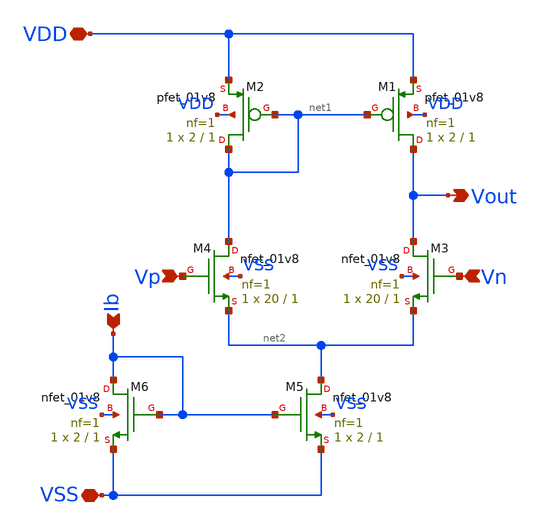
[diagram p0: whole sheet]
** sch_path: xschem/ota-5t.sch
**.subckt ota-5t Vp Vn Vout VDD VSS Ib
*.ipin Vp
*.ipin Vn
*.opin Vout
*.iopin VDD
*.iopin VSS
*.ipin Ib
XM4 net1 Vp net2 VSS sky130_fd_pr__nfet_01v8 L=1 W=20 nf=1 ad='int((1 + 1)/2) * 20 / 1 * 0.29' as='int((1 + 2)/2) * 20 / 1 * 0.29'
+ pd='2*int((1 + 1)/2) * (20 / 1 + 0.29)' ps='2*int((1 + 2)/2) * (20 / 1 + 0.29)' nrd='0.29 / 20 ' nrs='0.29 / 20 '
+ sa=0 sb=0 sd=0 mult=1 m=1
XM1 Vout net1 VDD VDD sky130_fd_pr__pfet_01v8 L=1 W=2 nf=1 ad='int((nf+1)/2) * W/nf * 0.29' as='int((nf+2)/2) * W/nf * 0.29'
+ pd='2*int((nf+1)/2) * (W/nf + 0.29)' ps='2*int((nf+2)/2) * (W/nf + 0.29)' nrd='0.29 / W' nrs='0.29 / W'
+ sa=0 sb=0 sd=0 mult=1 m=1
XM2 net1 net1 VDD VDD sky130_fd_pr__pfet_01v8 L=1 W=2 nf=1 ad='int((nf+1)/2) * W/nf * 0.29' as='int((nf+2)/2) * W/nf * 0.29'
+ pd='2*int((nf+1)/2) * (W/nf + 0.29)' ps='2*int((nf+2)/2) * (W/nf + 0.29)' nrd='0.29 / W' nrs='0.29 / W'
+ sa=0 sb=0 sd=0 mult=1 m=1
XM3 Vout Vn net2 VSS sky130_fd_pr__nfet_01v8 L=1 W=20 nf=1 ad='int((1 + 1)/2) * 20 / 1 * 0.29' as='int((1 + 2)/2) * 20 / 1 * 0.29'
+ pd='2*int((1 + 1)/2) * (20 / 1 + 0.29)' ps='2*int((1 + 2)/2) * (20 / 1 + 0.29)' nrd='0.29 / 20 ' nrs='0.29 / 20 '
+ sa=0 sb=0 sd=0 mult=1 m=1
XM5 net2 Ib VSS VSS sky130_fd_pr__nfet_01v8 L=1 W=2 nf=1 ad='int((1 + 1)/2) * 2 / 1 * 0.29' as='int((1 + 2)/2) * 2 / 1 * 0.29'
+ pd='2*int((1 + 1)/2) * (2 / 1 + 0.29)' ps='2*int((1 + 2)/2) * (2 / 1 + 0.29)' nrd='0.29 / 2 ' nrs='0.29 / 2 '
+ sa=0 sb=0 sd=0 mult=1 m=1
XM6 Ib Ib VSS VSS sky130_fd_pr__nfet_01v8 L=1 W=2 nf=1 ad='int((1 + 1)/2) * 2 / 1 * 0.29' as='int((1 + 2)/2) * 2 / 1 * 0.29'
+ pd='2*int((1 + 1)/2) * (2 / 1 + 0.29)' ps='2*int((1 + 2)/2) * (2 / 1 + 0.29)' nrd='0.29 / 2 ' nrs='0.29 / 2 '
+ sa=0 sb=0 sd=0 mult=1 m=1
**.ends
.end
